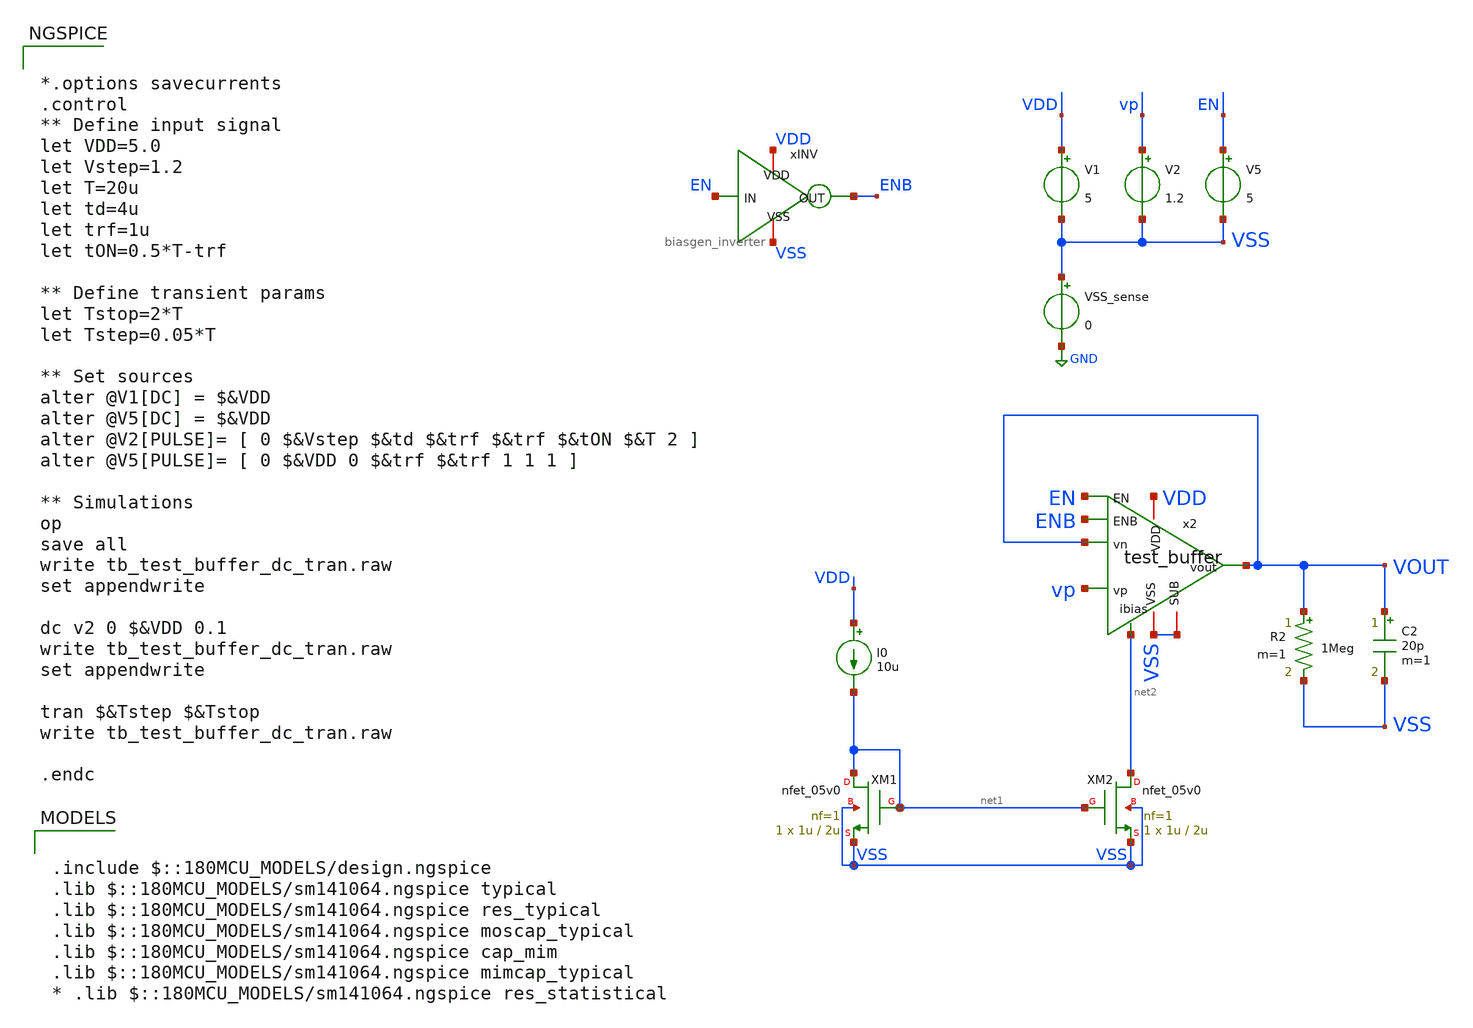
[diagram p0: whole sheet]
** sch_path: designs/libs/tb_test/tb_test_buffer_dc_tran/tb_test_buffer_dc_tran.sch
**.subckt tb_test_buffer_dc_tran
V1 VDD VSS 5
V2 vp VSS 1.2
VSS_sense VSS GND 0
I0 VDD net1 10u
xINV VDD EN ENB VSS biasgen_inverter
V5 EN VSS 5
XM1 net1 net1 VSS VSS nfet_05v0 L=2u W=1u nf=1 ad='int((nf+1)/2) * W/nf * 0.18u' as='int((nf+2)/2) * W/nf * 0.18u'
+ pd='2*int((nf+1)/2) * (W/nf + 0.18u)' ps='2*int((nf+2)/2) * (W/nf + 0.18u)' nrd='0.18u / W' nrs='0.18u / W'
+ sa=0 sb=0 sd=0 m=1
XM2 net2 net1 VSS VSS nfet_05v0 L=2u W=1u nf=1 ad='int((nf+1)/2) * W/nf * 0.18u' as='int((nf+2)/2) * W/nf * 0.18u'
+ pd='2*int((nf+1)/2) * (W/nf + 0.18u)' ps='2*int((nf+2)/2) * (W/nf + 0.18u)' nrd='0.18u / W' nrs='0.18u / W'
+ sa=0 sb=0 sd=0 m=1
C2 VOUT VSS 20p m=1
R2 VOUT VSS 1Meg m=1
x2 VDD net2 VOUT vp VOUT VSS EN ENB VSS test_buffer
**** begin user architecture code

.include $::180MCU_MODELS/design.ngspice
.lib $::180MCU_MODELS/sm141064.ngspice typical
.lib $::180MCU_MODELS/sm141064.ngspice res_typical
.lib $::180MCU_MODELS/sm141064.ngspice moscap_typical
.lib $::180MCU_MODELS/sm141064.ngspice cap_mim
.lib $::180MCU_MODELS/sm141064.ngspice mimcap_typical
* .lib $::180MCU_MODELS/sm141064.ngspice res_statistical



*.options savecurrents
.control
** Define input signal
let VDD=5.0
let Vstep=1.2
let T=20u
let td=4u
let trf=1u
let tON=0.5*T-trf

** Define transient params
let Tstop=2*T
let Tstep=0.05*T

** Set sources
alter @V1[DC] = $&VDD
alter @V5[DC] = $&VDD
alter @V2[PULSE]= [ 0 $&Vstep $&td $&trf $&trf $&tON $&T 2 ]
alter @V5[PULSE]= [ 0 $&VDD 0 $&trf $&trf 1 1 1 ]

** Simulations
op
save all
write tb_test_buffer_dc_tran.raw
set appendwrite

dc v2 0 $&VDD 0.1
write tb_test_buffer_dc_tran.raw
set appendwrite

tran $&Tstep $&Tstop
write tb_test_buffer_dc_tran.raw

.endc


**** end user architecture code
**.ends

* expanding   symbol:  libs/core_biasgen/biasgen_inverter/biasgen_inverter.sym # of pins=4
** sym_path: designs/libs/core_biasgen/biasgen_inverter/biasgen_inverter.sym
** sch_path: designs/libs/core_biasgen/biasgen_inverter/biasgen_inverter.sch
.subckt biasgen_inverter VDD IN OUT VSS
*.iopin VDD
*.iopin VSS
*.ipin IN
*.opin OUT
XMINV1 OUT IN VSS VSS nfet_05v0 L=0.60u W=0.50u nf=1 ad='int((nf+1)/2) * W/nf * 0.18u' as='int((nf+2)/2) * W/nf * 0.18u'
+ pd='2*int((nf+1)/2) * (W/nf + 0.18u)' ps='2*int((nf+2)/2) * (W/nf + 0.18u)' nrd='0.18u / W' nrs='0.18u / W'
+ sa=0 sb=0 sd=0 m=1
XMINV2 OUT IN VDD VDD pfet_05v0 L=0.50u W=0.60u nf=1 ad='int((nf+1)/2) * W/nf * 0.18u' as='int((nf+2)/2) * W/nf * 0.18u'
+ pd='2*int((nf+1)/2) * (W/nf + 0.18u)' ps='2*int((nf+2)/2) * (W/nf + 0.18u)' nrd='0.18u / W' nrs='0.18u / W'
+ sa=0 sb=0 sd=0 m=1
.ends


* expanding   symbol:  libs/core_test/test_buffer/test_buffer.sym # of pins=9
** sym_path: designs/libs/core_test/test_buffer/test_buffer.sym
** sch_path: designs/libs/core_test/test_buffer/test_buffer.sch
.subckt test_buffer VDD ibias vn vp vout VSS EN ENB SUB
*.ipin vn
*.ipin vp
*.opin vout
*.ipin ibias
*.iopin VDD
*.iopin VSS
*.ipin EN
*.ipin ENB
*.iopin SUB
XCM net1 vout_1st cap_nmos_03v3_b c_width=15u c_length=15u m=1
XMpref0 vpref vpref VDD VDD pfet_05v0 L=1u W=0.5u nf=1 ad='int((nf+1)/2) * W/nf * 0.18u' as='int((nf+2)/2) * W/nf * 0.18u'
+ pd='2*int((nf+1)/2) * (W/nf + 0.18u)' ps='2*int((nf+2)/2) * (W/nf + 0.18u)' nrd='0.18u / W' nrs='0.18u / W'
+ sa=0 sb=0 sd=0 m=10
XMnload0 vnload vnload VSS VSS nfet_05v0 L=2u W=0.5u nf=1 ad='int((nf+1)/2) * W/nf * 0.18u' as='int((nf+2)/2) * W/nf * 0.18u'
+ pd='2*int((nf+1)/2) * (W/nf + 0.18u)' ps='2*int((nf+2)/2) * (W/nf + 0.18u)' nrd='0.18u / W' nrs='0.18u / W'
+ sa=0 sb=0 sd=0 m=2
XMpref1 vptail vpref VDD VDD pfet_05v0 L=1u W=0.5u nf=1 ad='int((nf+1)/2) * W/nf * 0.18u' as='int((nf+2)/2) * W/nf * 0.18u'
+ pd='2*int((nf+1)/2) * (W/nf + 0.18u)' ps='2*int((nf+2)/2) * (W/nf + 0.18u)' nrd='0.18u / W' nrs='0.18u / W'
+ sa=0 sb=0 sd=0 m=2
XMpref2 net1 vpref VDD VDD pfet_05v0 L=1u W=0.5u nf=1 ad='int((nf+1)/2) * W/nf * 0.18u' as='int((nf+2)/2) * W/nf * 0.18u'
+ pd='2*int((nf+1)/2) * (W/nf + 0.18u)' ps='2*int((nf+2)/2) * (W/nf + 0.18u)' nrd='0.18u / W' nrs='0.18u / W'
+ sa=0 sb=0 sd=0 m=16
XMpdiff0 vnload vn vptail VDD pfet_05v0 L=1u W=2u nf=1 ad='int((nf+1)/2) * W/nf * 0.18u' as='int((nf+2)/2) * W/nf * 0.18u'
+ pd='2*int((nf+1)/2) * (W/nf + 0.18u)' ps='2*int((nf+2)/2) * (W/nf + 0.18u)' nrd='0.18u / W' nrs='0.18u / W'
+ sa=0 sb=0 sd=0 m=2
XMpdiff1 vout_1st vp vptail VDD pfet_05v0 L=1u W=2u nf=1 ad='int((nf+1)/2) * W/nf * 0.18u' as='int((nf+2)/2) * W/nf * 0.18u'
+ pd='2*int((nf+1)/2) * (W/nf + 0.18u)' ps='2*int((nf+2)/2) * (W/nf + 0.18u)' nrd='0.18u / W' nrs='0.18u / W'
+ sa=0 sb=0 sd=0 m=2
XMnload1 vout_1st vnload VSS VSS nfet_05v0 L=2u W=0.5u nf=1 ad='int((nf+1)/2) * W/nf * 0.18u' as='int((nf+2)/2) * W/nf * 0.18u'
+ pd='2*int((nf+1)/2) * (W/nf + 0.18u)' ps='2*int((nf+2)/2) * (W/nf + 0.18u)' nrd='0.18u / W' nrs='0.18u / W'
+ sa=0 sb=0 sd=0 m=2
XMncs net1 vout_1st VSS VSS nfet_05v0 L=2u W=0.5u nf=1 ad='int((nf+1)/2) * W/nf * 0.18u' as='int((nf+2)/2) * W/nf * 0.18u'
+ pd='2*int((nf+1)/2) * (W/nf + 0.18u)' ps='2*int((nf+2)/2) * (W/nf + 0.18u)' nrd='0.18u / W' nrs='0.18u / W'
+ sa=0 sb=0 sd=0 m=32
XMpref_dumm_L[3] VDD VDD VDD VDD pfet_05v0 L=1u W=0.5u nf=1 ad='int((nf+1)/2) * W/nf * 0.18u' as='int((nf+2)/2) * W/nf * 0.18u'
+ pd='2*int((nf+1)/2) * (W/nf + 0.18u)' ps='2*int((nf+2)/2) * (W/nf + 0.18u)' nrd='0.18u / W' nrs='0.18u / W'
+ sa=0 sb=0 sd=0 m=1
XMpref_dumm_L[2] VDD VDD VDD VDD pfet_05v0 L=1u W=0.5u nf=1 ad='int((nf+1)/2) * W/nf * 0.18u' as='int((nf+2)/2) * W/nf * 0.18u'
+ pd='2*int((nf+1)/2) * (W/nf + 0.18u)' ps='2*int((nf+2)/2) * (W/nf + 0.18u)' nrd='0.18u / W' nrs='0.18u / W'
+ sa=0 sb=0 sd=0 m=1
XMpref_dumm_L[1] VDD VDD VDD VDD pfet_05v0 L=1u W=0.5u nf=1 ad='int((nf+1)/2) * W/nf * 0.18u' as='int((nf+2)/2) * W/nf * 0.18u'
+ pd='2*int((nf+1)/2) * (W/nf + 0.18u)' ps='2*int((nf+2)/2) * (W/nf + 0.18u)' nrd='0.18u / W' nrs='0.18u / W'
+ sa=0 sb=0 sd=0 m=1
XMpref_dumm_L[0] VDD VDD VDD VDD pfet_05v0 L=1u W=0.5u nf=1 ad='int((nf+1)/2) * W/nf * 0.18u' as='int((nf+2)/2) * W/nf * 0.18u'
+ pd='2*int((nf+1)/2) * (W/nf + 0.18u)' ps='2*int((nf+2)/2) * (W/nf + 0.18u)' nrd='0.18u / W' nrs='0.18u / W'
+ sa=0 sb=0 sd=0 m=1
XMpref_dumm_TP[23] VDD VDD VDD VDD pfet_05v0 L=1u W=0.5u nf=1 ad='int((nf+1)/2) * W/nf * 0.18u' as='int((nf+2)/2) * W/nf * 0.18u'
+ pd='2*int((nf+1)/2) * (W/nf + 0.18u)' ps='2*int((nf+2)/2) * (W/nf + 0.18u)' nrd='0.18u / W' nrs='0.18u / W'
+ sa=0 sb=0 sd=0 m=1
XMpref_dumm_TP[22] VDD VDD VDD VDD pfet_05v0 L=1u W=0.5u nf=1 ad='int((nf+1)/2) * W/nf * 0.18u' as='int((nf+2)/2) * W/nf * 0.18u'
+ pd='2*int((nf+1)/2) * (W/nf + 0.18u)' ps='2*int((nf+2)/2) * (W/nf + 0.18u)' nrd='0.18u / W' nrs='0.18u / W'
+ sa=0 sb=0 sd=0 m=1
XMpref_dumm_TP[21] VDD VDD VDD VDD pfet_05v0 L=1u W=0.5u nf=1 ad='int((nf+1)/2) * W/nf * 0.18u' as='int((nf+2)/2) * W/nf * 0.18u'
+ pd='2*int((nf+1)/2) * (W/nf + 0.18u)' ps='2*int((nf+2)/2) * (W/nf + 0.18u)' nrd='0.18u / W' nrs='0.18u / W'
+ sa=0 sb=0 sd=0 m=1
XMpref_dumm_TP[20] VDD VDD VDD VDD pfet_05v0 L=1u W=0.5u nf=1 ad='int((nf+1)/2) * W/nf * 0.18u' as='int((nf+2)/2) * W/nf * 0.18u'
+ pd='2*int((nf+1)/2) * (W/nf + 0.18u)' ps='2*int((nf+2)/2) * (W/nf + 0.18u)' nrd='0.18u / W' nrs='0.18u / W'
+ sa=0 sb=0 sd=0 m=1
XMpref_dumm_TP[19] VDD VDD VDD VDD pfet_05v0 L=1u W=0.5u nf=1 ad='int((nf+1)/2) * W/nf * 0.18u' as='int((nf+2)/2) * W/nf * 0.18u'
+ pd='2*int((nf+1)/2) * (W/nf + 0.18u)' ps='2*int((nf+2)/2) * (W/nf + 0.18u)' nrd='0.18u / W' nrs='0.18u / W'
+ sa=0 sb=0 sd=0 m=1
XMpref_dumm_TP[18] VDD VDD VDD VDD pfet_05v0 L=1u W=0.5u nf=1 ad='int((nf+1)/2) * W/nf * 0.18u' as='int((nf+2)/2) * W/nf * 0.18u'
+ pd='2*int((nf+1)/2) * (W/nf + 0.18u)' ps='2*int((nf+2)/2) * (W/nf + 0.18u)' nrd='0.18u / W' nrs='0.18u / W'
+ sa=0 sb=0 sd=0 m=1
XMpref_dumm_TP[17] VDD VDD VDD VDD pfet_05v0 L=1u W=0.5u nf=1 ad='int((nf+1)/2) * W/nf * 0.18u' as='int((nf+2)/2) * W/nf * 0.18u'
+ pd='2*int((nf+1)/2) * (W/nf + 0.18u)' ps='2*int((nf+2)/2) * (W/nf + 0.18u)' nrd='0.18u / W' nrs='0.18u / W'
+ sa=0 sb=0 sd=0 m=1
XMpref_dumm_TP[16] VDD VDD VDD VDD pfet_05v0 L=1u W=0.5u nf=1 ad='int((nf+1)/2) * W/nf * 0.18u' as='int((nf+2)/2) * W/nf * 0.18u'
+ pd='2*int((nf+1)/2) * (W/nf + 0.18u)' ps='2*int((nf+2)/2) * (W/nf + 0.18u)' nrd='0.18u / W' nrs='0.18u / W'
+ sa=0 sb=0 sd=0 m=1
XMpref_dumm_TP[15] VDD VDD VDD VDD pfet_05v0 L=1u W=0.5u nf=1 ad='int((nf+1)/2) * W/nf * 0.18u' as='int((nf+2)/2) * W/nf * 0.18u'
+ pd='2*int((nf+1)/2) * (W/nf + 0.18u)' ps='2*int((nf+2)/2) * (W/nf + 0.18u)' nrd='0.18u / W' nrs='0.18u / W'
+ sa=0 sb=0 sd=0 m=1
XMpref_dumm_TP[14] VDD VDD VDD VDD pfet_05v0 L=1u W=0.5u nf=1 ad='int((nf+1)/2) * W/nf * 0.18u' as='int((nf+2)/2) * W/nf * 0.18u'
+ pd='2*int((nf+1)/2) * (W/nf + 0.18u)' ps='2*int((nf+2)/2) * (W/nf + 0.18u)' nrd='0.18u / W' nrs='0.18u / W'
+ sa=0 sb=0 sd=0 m=1
XMpref_dumm_TP[13] VDD VDD VDD VDD pfet_05v0 L=1u W=0.5u nf=1 ad='int((nf+1)/2) * W/nf * 0.18u' as='int((nf+2)/2) * W/nf * 0.18u'
+ pd='2*int((nf+1)/2) * (W/nf + 0.18u)' ps='2*int((nf+2)/2) * (W/nf + 0.18u)' nrd='0.18u / W' nrs='0.18u / W'
+ sa=0 sb=0 sd=0 m=1
XMpref_dumm_TP[12] VDD VDD VDD VDD pfet_05v0 L=1u W=0.5u nf=1 ad='int((nf+1)/2) * W/nf * 0.18u' as='int((nf+2)/2) * W/nf * 0.18u'
+ pd='2*int((nf+1)/2) * (W/nf + 0.18u)' ps='2*int((nf+2)/2) * (W/nf + 0.18u)' nrd='0.18u / W' nrs='0.18u / W'
+ sa=0 sb=0 sd=0 m=1
XMpref_dumm_TP[11] VDD VDD VDD VDD pfet_05v0 L=1u W=0.5u nf=1 ad='int((nf+1)/2) * W/nf * 0.18u' as='int((nf+2)/2) * W/nf * 0.18u'
+ pd='2*int((nf+1)/2) * (W/nf + 0.18u)' ps='2*int((nf+2)/2) * (W/nf + 0.18u)' nrd='0.18u / W' nrs='0.18u / W'
+ sa=0 sb=0 sd=0 m=1
XMpref_dumm_TP[10] VDD VDD VDD VDD pfet_05v0 L=1u W=0.5u nf=1 ad='int((nf+1)/2) * W/nf * 0.18u' as='int((nf+2)/2) * W/nf * 0.18u'
+ pd='2*int((nf+1)/2) * (W/nf + 0.18u)' ps='2*int((nf+2)/2) * (W/nf + 0.18u)' nrd='0.18u / W' nrs='0.18u / W'
+ sa=0 sb=0 sd=0 m=1
XMpref_dumm_TP[9] VDD VDD VDD VDD pfet_05v0 L=1u W=0.5u nf=1 ad='int((nf+1)/2) * W/nf * 0.18u' as='int((nf+2)/2) * W/nf * 0.18u'
+ pd='2*int((nf+1)/2) * (W/nf + 0.18u)' ps='2*int((nf+2)/2) * (W/nf + 0.18u)' nrd='0.18u / W' nrs='0.18u / W'
+ sa=0 sb=0 sd=0 m=1
XMpref_dumm_TP[8] VDD VDD VDD VDD pfet_05v0 L=1u W=0.5u nf=1 ad='int((nf+1)/2) * W/nf * 0.18u' as='int((nf+2)/2) * W/nf * 0.18u'
+ pd='2*int((nf+1)/2) * (W/nf + 0.18u)' ps='2*int((nf+2)/2) * (W/nf + 0.18u)' nrd='0.18u / W' nrs='0.18u / W'
+ sa=0 sb=0 sd=0 m=1
XMpref_dumm_TP[7] VDD VDD VDD VDD pfet_05v0 L=1u W=0.5u nf=1 ad='int((nf+1)/2) * W/nf * 0.18u' as='int((nf+2)/2) * W/nf * 0.18u'
+ pd='2*int((nf+1)/2) * (W/nf + 0.18u)' ps='2*int((nf+2)/2) * (W/nf + 0.18u)' nrd='0.18u / W' nrs='0.18u / W'
+ sa=0 sb=0 sd=0 m=1
XMpref_dumm_TP[6] VDD VDD VDD VDD pfet_05v0 L=1u W=0.5u nf=1 ad='int((nf+1)/2) * W/nf * 0.18u' as='int((nf+2)/2) * W/nf * 0.18u'
+ pd='2*int((nf+1)/2) * (W/nf + 0.18u)' ps='2*int((nf+2)/2) * (W/nf + 0.18u)' nrd='0.18u / W' nrs='0.18u / W'
+ sa=0 sb=0 sd=0 m=1
XMpref_dumm_TP[5] VDD VDD VDD VDD pfet_05v0 L=1u W=0.5u nf=1 ad='int((nf+1)/2) * W/nf * 0.18u' as='int((nf+2)/2) * W/nf * 0.18u'
+ pd='2*int((nf+1)/2) * (W/nf + 0.18u)' ps='2*int((nf+2)/2) * (W/nf + 0.18u)' nrd='0.18u / W' nrs='0.18u / W'
+ sa=0 sb=0 sd=0 m=1
XMpref_dumm_TP[4] VDD VDD VDD VDD pfet_05v0 L=1u W=0.5u nf=1 ad='int((nf+1)/2) * W/nf * 0.18u' as='int((nf+2)/2) * W/nf * 0.18u'
+ pd='2*int((nf+1)/2) * (W/nf + 0.18u)' ps='2*int((nf+2)/2) * (W/nf + 0.18u)' nrd='0.18u / W' nrs='0.18u / W'
+ sa=0 sb=0 sd=0 m=1
XMpref_dumm_TP[3] VDD VDD VDD VDD pfet_05v0 L=1u W=0.5u nf=1 ad='int((nf+1)/2) * W/nf * 0.18u' as='int((nf+2)/2) * W/nf * 0.18u'
+ pd='2*int((nf+1)/2) * (W/nf + 0.18u)' ps='2*int((nf+2)/2) * (W/nf + 0.18u)' nrd='0.18u / W' nrs='0.18u / W'
+ sa=0 sb=0 sd=0 m=1
XMpref_dumm_TP[2] VDD VDD VDD VDD pfet_05v0 L=1u W=0.5u nf=1 ad='int((nf+1)/2) * W/nf * 0.18u' as='int((nf+2)/2) * W/nf * 0.18u'
+ pd='2*int((nf+1)/2) * (W/nf + 0.18u)' ps='2*int((nf+2)/2) * (W/nf + 0.18u)' nrd='0.18u / W' nrs='0.18u / W'
+ sa=0 sb=0 sd=0 m=1
XMpref_dumm_TP[1] VDD VDD VDD VDD pfet_05v0 L=1u W=0.5u nf=1 ad='int((nf+1)/2) * W/nf * 0.18u' as='int((nf+2)/2) * W/nf * 0.18u'
+ pd='2*int((nf+1)/2) * (W/nf + 0.18u)' ps='2*int((nf+2)/2) * (W/nf + 0.18u)' nrd='0.18u / W' nrs='0.18u / W'
+ sa=0 sb=0 sd=0 m=1
XMpref_dumm_TP[0] VDD VDD VDD VDD pfet_05v0 L=1u W=0.5u nf=1 ad='int((nf+1)/2) * W/nf * 0.18u' as='int((nf+2)/2) * W/nf * 0.18u'
+ pd='2*int((nf+1)/2) * (W/nf + 0.18u)' ps='2*int((nf+2)/2) * (W/nf + 0.18u)' nrd='0.18u / W' nrs='0.18u / W'
+ sa=0 sb=0 sd=0 m=1
XMpenpref vpref EN VDD VDD pfet_05v0 L=0.5u W=1u nf=1 ad='int((nf+1)/2) * W/nf * 0.18u' as='int((nf+2)/2) * W/nf * 0.18u'
+ pd='2*int((nf+1)/2) * (W/nf + 0.18u)' ps='2*int((nf+2)/2) * (W/nf + 0.18u)' nrd='0.18u / W' nrs='0.18u / W'
+ sa=0 sb=0 sd=0 m=1
XMpenbias ibias ENB vpref VDD pfet_05v0 L=0.5u W=1u nf=1 ad='int((nf+1)/2) * W/nf * 0.18u' as='int((nf+2)/2) * W/nf * 0.18u'
+ pd='2*int((nf+1)/2) * (W/nf + 0.18u)' ps='2*int((nf+2)/2) * (W/nf + 0.18u)' nrd='0.18u / W' nrs='0.18u / W'
+ sa=0 sb=0 sd=0 m=5
XMnennref vnload ENB VSS VSS nfet_05v0 L=0.6u W=2u nf=1 ad='int((nf+1)/2) * W/nf * 0.18u' as='int((nf+2)/2) * W/nf * 0.18u'
+ pd='2*int((nf+1)/2) * (W/nf + 0.18u)' ps='2*int((nf+2)/2) * (W/nf + 0.18u)' nrd='0.18u / W' nrs='0.18u / W'
+ sa=0 sb=0 sd=0 m=1
XMnennref1 vout_1st ENB VSS VSS nfet_05v0 L=0.6u W=2u nf=1 ad='int((nf+1)/2) * W/nf * 0.18u' as='int((nf+2)/2) * W/nf * 0.18u'
+ pd='2*int((nf+1)/2) * (W/nf + 0.18u)' ps='2*int((nf+2)/2) * (W/nf + 0.18u)' nrd='0.18u / W' nrs='0.18u / W'
+ sa=0 sb=0 sd=0 m=1
* noconn SUB
XMpref3 net2 vpref VDD VDD pfet_05v0 L=1u W=0.5u nf=1 ad='int((nf+1)/2) * W/nf * 0.18u' as='int((nf+2)/2) * W/nf * 0.18u'
+ pd='2*int((nf+1)/2) * (W/nf + 0.18u)' ps='2*int((nf+2)/2) * (W/nf + 0.18u)' nrd='0.18u / W' nrs='0.18u / W'
+ sa=0 sb=0 sd=0 m=2
XMnbias0 net2 net2 VSS VSS nfet_05v0 L=2u W=0.5u nf=1 ad='int((nf+1)/2) * W/nf * 0.18u' as='int((nf+2)/2) * W/nf * 0.18u'
+ pd='2*int((nf+1)/2) * (W/nf + 0.18u)' ps='2*int((nf+2)/2) * (W/nf + 0.18u)' nrd='0.18u / W' nrs='0.18u / W'
+ sa=0 sb=0 sd=0 m=2
XMnbias1 vout net2 VSS VSS nfet_05v0 L=2u W=0.5u nf=1 ad='int((nf+1)/2) * W/nf * 0.18u' as='int((nf+2)/2) * W/nf * 0.18u'
+ pd='2*int((nf+1)/2) * (W/nf + 0.18u)' ps='2*int((nf+2)/2) * (W/nf + 0.18u)' nrd='0.18u / W' nrs='0.18u / W'
+ sa=0 sb=0 sd=0 m=64
XMnsf VDD net1 vout vout nfet_05v0 L=1u W=0.5u nf=1 ad='int((nf+1)/2) * W/nf * 0.18u' as='int((nf+2)/2) * W/nf * 0.18u'
+ pd='2*int((nf+1)/2) * (W/nf + 0.18u)' ps='2*int((nf+2)/2) * (W/nf + 0.18u)' nrd='0.18u / W' nrs='0.18u / W'
+ sa=0 sb=0 sd=0 m=64
XMnennref2 net2 ENB VSS VSS nfet_05v0 L=0.6u W=2u nf=1 ad='int((nf+1)/2) * W/nf * 0.18u' as='int((nf+2)/2) * W/nf * 0.18u'
+ pd='2*int((nf+1)/2) * (W/nf + 0.18u)' ps='2*int((nf+2)/2) * (W/nf + 0.18u)' nrd='0.18u / W' nrs='0.18u / W'
+ sa=0 sb=0 sd=0 m=1
XMnennref3 net1 ENB VSS VSS nfet_05v0 L=0.6u W=2u nf=1 ad='int((nf+1)/2) * W/nf * 0.18u' as='int((nf+2)/2) * W/nf * 0.18u'
+ pd='2*int((nf+1)/2) * (W/nf + 0.18u)' ps='2*int((nf+2)/2) * (W/nf + 0.18u)' nrd='0.18u / W' nrs='0.18u / W'
+ sa=0 sb=0 sd=0 m=1
.ends

.GLOBAL GND
.end
